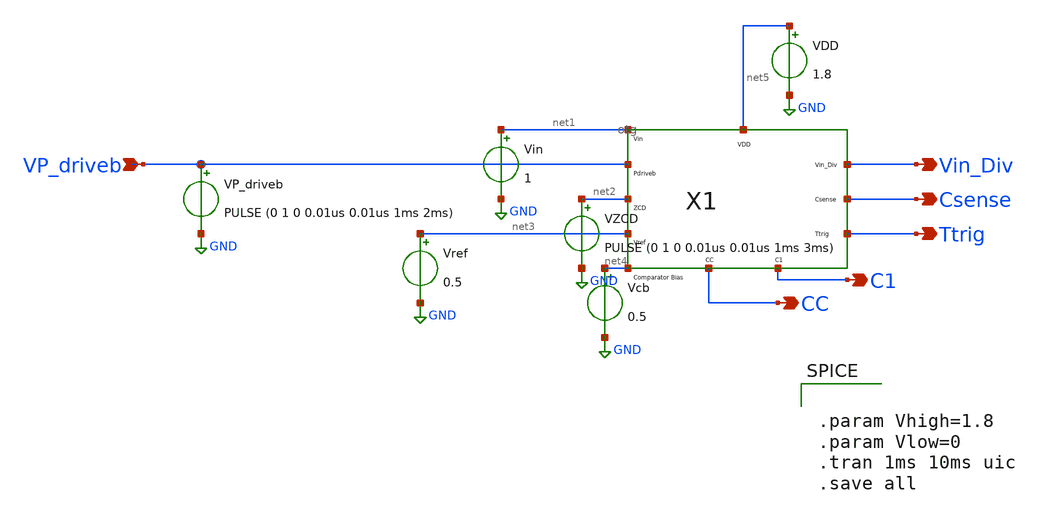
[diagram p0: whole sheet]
** sch_path: Current Sensor/otg_testing.sch
**.subckt otg_testing Vin_Div Csense Ttrig VP_driveb CC C1
*.opin Vin_Div
*.opin Csense
*.opin Ttrig
*.ipin VP_driveb
*.opin CC
*.opin C1
X1 net1 VP_driveb net2 net3 net4 net5 Vin_Div Csense Ttrig CC C1 otg
Vin net1 GND 1
Vref net3 GND 0.5
VDD net5 GND 1.8
Vcb net4 GND 0.5
VP_driveb VP_driveb GND PULSE (0 1 0 0.01us 0.01us 1ms 2ms)
VZCD net2 GND PULSE (0 1 0 0.01us 0.01us 1ms 3ms)
**** begin user architecture code


.param Vhigh=1.8
.param Vlow=0
.tran 1ms 10ms uic
.save all


** opencircuitdesign pdks install
.lib $::SKYWATER_MODELS/sky130.lib.spice tt_mm


**** end user architecture code
**.ends
.GLOBAL GND
.end
